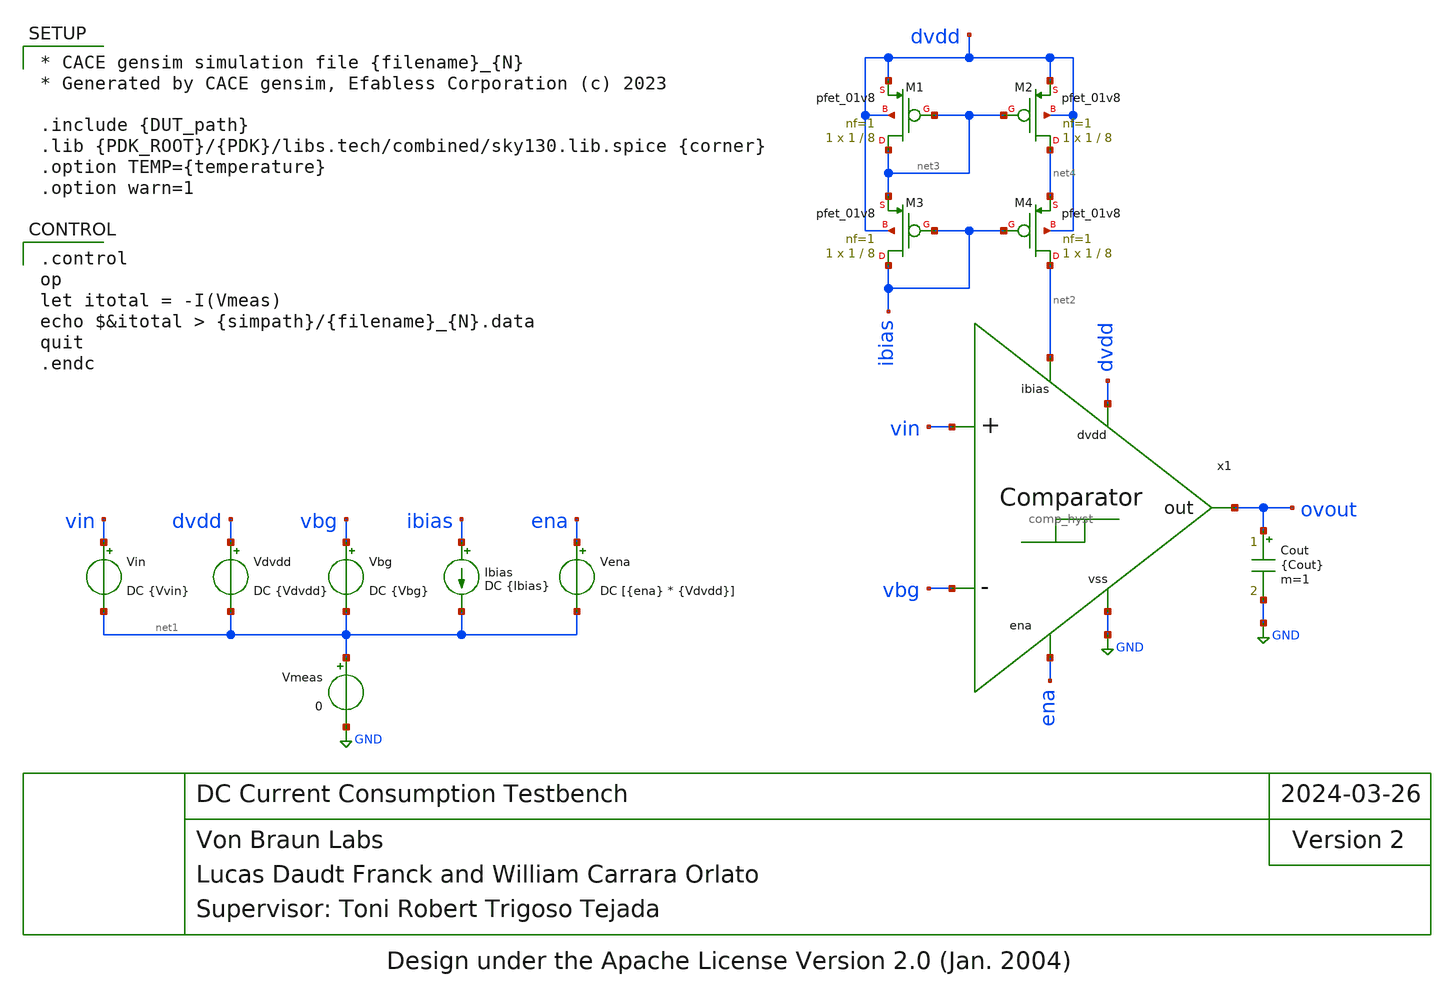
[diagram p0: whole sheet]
** sch_path: blocks/comp_hyst/cace/tb_dccurrent.sch
* Design under the Apache License Version 2.0 (Jan. 2004)
**.subckt tb_dccurrent
Cout ovout GND {Cout} m=1
Vin vin net1 DC {Vvin}
Vdvdd dvdd net1 DC {Vdvdd}
Vena ena net1 DC [{ena} * {Vdvdd}]
Vbg vbg net1 DC {Vbg}
Ibias ibias net1 DC {Ibias}
Vmeas net1 GND 0
XM1 net3 net3 dvdd dvdd sky130_fd_pr__pfet_01v8 L=8 W=1 nf=1 ad='int((nf+1)/2) * W/nf * 0.29' as='int((nf+2)/2) * W/nf * 0.29'
+ pd='2*int((nf+1)/2) * (W/nf + 0.29)' ps='2*int((nf+2)/2) * (W/nf + 0.29)' nrd='0.29 / W' nrs='0.29 / W'
+ sa=0 sb=0 sd=0 mult=1 m=1
XM2 net4 net3 dvdd dvdd sky130_fd_pr__pfet_01v8 L=8 W=1 nf=1 ad='int((nf+1)/2) * W/nf * 0.29' as='int((nf+2)/2) * W/nf * 0.29'
+ pd='2*int((nf+1)/2) * (W/nf + 0.29)' ps='2*int((nf+2)/2) * (W/nf + 0.29)' nrd='0.29 / W' nrs='0.29 / W'
+ sa=0 sb=0 sd=0 mult=1 m=1
XM3 ibias ibias net3 dvdd sky130_fd_pr__pfet_01v8 L=8 W=1 nf=1 ad='int((nf+1)/2) * W/nf * 0.29' as='int((nf+2)/2) * W/nf * 0.29'
+ pd='2*int((nf+1)/2) * (W/nf + 0.29)' ps='2*int((nf+2)/2) * (W/nf + 0.29)' nrd='0.29 / W' nrs='0.29 / W'
+ sa=0 sb=0 sd=0 mult=1 m=1
XM4 net2 ibias net4 dvdd sky130_fd_pr__pfet_01v8 L=8 W=1 nf=1 ad='int((nf+1)/2) * W/nf * 0.29' as='int((nf+2)/2) * W/nf * 0.29'
+ pd='2*int((nf+1)/2) * (W/nf + 0.29)' ps='2*int((nf+2)/2) * (W/nf + 0.29)' nrd='0.29 / W' nrs='0.29 / W'
+ sa=0 sb=0 sd=0 mult=1 m=1
x1 dvdd ovout vbg vin ena net2 GND comp_hyst
**** begin user architecture code

* CACE gensim simulation file {filename}_{N}
* Generated by CACE gensim, Efabless Corporation (c) 2023

.include {DUT_path}
.lib {PDK_ROOT}/{PDK}/libs.tech/combined/sky130.lib.spice {corner}
.option TEMP={temperature}
.option warn=1



.control
op
let itotal = -I(Vmeas)
echo $&itotal > {simpath}/{filename}_{N}.data
quit
.endc


**** end user architecture code
**.ends

* expanding   symbol:
*+  /home/vblabs/Music/sky130_vbl_ip__overvoltage/blocks/comp_hyst/xschem/comp_hyst.sym # of pins=7
** sym_path: blocks/comp_hyst/xschem/comp_hyst.sym
** sch_path: blocks/comp_hyst/xschem/comp_hyst.sch
.subckt comp_hyst dvdd out vref vin ena ibias vss
*.iopin dvdd
*.ipin vref
*.ipin vin
*.opin out
*.ipin ibias
*.ipin ena
*.iopin vss
XM5[0] net3 net4 dvdd dvdd sky130_fd_pr__pfet_01v8 L=8 W=1 nf=1 ad='int((nf+1)/2) * W/nf * 0.29' as='int((nf+2)/2) * W/nf * 0.29'
+ pd='2*int((nf+1)/2) * (W/nf + 0.29)' ps='2*int((nf+2)/2) * (W/nf + 0.29)' nrd='0.29 / W' nrs='0.29 / W'
+ sa=0 sb=0 sd=0 mult=1 m=1
XM5[1] net3 net4 dvdd dvdd sky130_fd_pr__pfet_01v8 L=8 W=1 nf=1 ad='int((nf+1)/2) * W/nf * 0.29' as='int((nf+2)/2) * W/nf * 0.29'
+ pd='2*int((nf+1)/2) * (W/nf + 0.29)' ps='2*int((nf+2)/2) * (W/nf + 0.29)' nrd='0.29 / W' nrs='0.29 / W'
+ sa=0 sb=0 sd=0 mult=1 m=1
XM2[0] net4 net4 dvdd dvdd sky130_fd_pr__pfet_01v8 L=8 W=1 nf=1 ad='int((nf+1)/2) * W/nf * 0.29' as='int((nf+2)/2) * W/nf * 0.29'
+ pd='2*int((nf+1)/2) * (W/nf + 0.29)' ps='2*int((nf+2)/2) * (W/nf + 0.29)' nrd='0.29 / W' nrs='0.29 / W'
+ sa=0 sb=0 sd=0 mult=1 m=1
XM2[1] net4 net4 dvdd dvdd sky130_fd_pr__pfet_01v8 L=8 W=1 nf=1 ad='int((nf+1)/2) * W/nf * 0.29' as='int((nf+2)/2) * W/nf * 0.29'
+ pd='2*int((nf+1)/2) * (W/nf + 0.29)' ps='2*int((nf+2)/2) * (W/nf + 0.29)' nrd='0.29 / W' nrs='0.29 / W'
+ sa=0 sb=0 sd=0 mult=1 m=1
XM8 net2 net4 dvdd dvdd sky130_fd_pr__pfet_01v8 L=8 W=1 nf=1 ad='int((nf+1)/2) * W/nf * 0.29' as='int((nf+2)/2) * W/nf * 0.29'
+ pd='2*int((nf+1)/2) * (W/nf + 0.29)' ps='2*int((nf+2)/2) * (W/nf + 0.29)' nrd='0.29 / W' nrs='0.29 / W'
+ sa=0 sb=0 sd=0 mult=1 m=1
XM10[0] net3 net3 dvdd dvdd sky130_fd_pr__pfet_01v8 L=16 W=1 nf=1 ad='int((nf+1)/2) * W/nf * 0.29' as='int((nf+2)/2) * W/nf * 0.29'
+ pd='2*int((nf+1)/2) * (W/nf + 0.29)' ps='2*int((nf+2)/2) * (W/nf + 0.29)' nrd='0.29 / W' nrs='0.29 / W'
+ sa=0 sb=0 sd=0 mult=1 m=1
XM10[1] net3 net3 dvdd dvdd sky130_fd_pr__pfet_01v8 L=16 W=1 nf=1 ad='int((nf+1)/2) * W/nf * 0.29' as='int((nf+2)/2) * W/nf * 0.29'
+ pd='2*int((nf+1)/2) * (W/nf + 0.29)' ps='2*int((nf+2)/2) * (W/nf + 0.29)' nrd='0.29 / W' nrs='0.29 / W'
+ sa=0 sb=0 sd=0 mult=1 m=1
XM11 net5 net5 vss vss sky130_fd_pr__nfet_01v8 L=20 W=1 nf=1 ad='int((nf+1)/2) * W/nf * 0.29' as='int((nf+2)/2) * W/nf * 0.29'
+ pd='2*int((nf+1)/2) * (W/nf + 0.29)' ps='2*int((nf+2)/2) * (W/nf + 0.29)' nrd='0.29 / W' nrs='0.29 / W'
+ sa=0 sb=0 sd=0 mult=1 m=1
XM12 net1 net5 vss vss sky130_fd_pr__nfet_01v8 L=20 W=1 nf=1 ad='int((nf+1)/2) * W/nf * 0.29' as='int((nf+2)/2) * W/nf * 0.29'
+ pd='2*int((nf+1)/2) * (W/nf + 0.29)' ps='2*int((nf+2)/2) * (W/nf + 0.29)' nrd='0.29 / W' nrs='0.29 / W'
+ sa=0 sb=0 sd=0 mult=1 m=1
XM4 out net3 dvdd dvdd sky130_fd_pr__pfet_01v8 L=1 W=3 nf=1 ad='int((nf+1)/2) * W/nf * 0.29' as='int((nf+2)/2) * W/nf * 0.29'
+ pd='2*int((nf+1)/2) * (W/nf + 0.29)' ps='2*int((nf+2)/2) * (W/nf + 0.29)' nrd='0.29 / W' nrs='0.29 / W'
+ sa=0 sb=0 sd=0 mult=1 m=1
XM13 out net2 vss vss sky130_fd_pr__nfet_01v8 L=1 W=3 nf=1 ad='int((nf+1)/2) * W/nf * 0.29' as='int((nf+2)/2) * W/nf * 0.29'
+ pd='2*int((nf+1)/2) * (W/nf + 0.29)' ps='2*int((nf+2)/2) * (W/nf + 0.29)' nrd='0.29 / W' nrs='0.29 / W'
+ sa=0 sb=0 sd=0 mult=1 m=1
XM20 out ena_b vss vss sky130_fd_pr__nfet_01v8 L=3 W=1 nf=1 ad='int((nf+1)/2) * W/nf * 0.29' as='int((nf+2)/2) * W/nf * 0.29'
+ pd='2*int((nf+1)/2) * (W/nf + 0.29)' ps='2*int((nf+2)/2) * (W/nf + 0.29)' nrd='0.29 / W' nrs='0.29 / W'
+ sa=0 sb=0 sd=0 mult=1 m=1
XM3[0] net4 vref net1 vss sky130_fd_pr__nfet_g5v0d10v5 L=8 W=1.3 nf=1 ad='int((nf+1)/2) * W/nf * 0.29'
+ as='int((nf+2)/2) * W/nf * 0.29' pd='2*int((nf+1)/2) * (W/nf + 0.29)' ps='2*int((nf+2)/2) * (W/nf + 0.29)'
+ nrd='0.29 / W' nrs='0.29 / W' sa=0 sb=0 sd=0 mult=1 m=1
XM3[1] net4 vref net1 vss sky130_fd_pr__nfet_g5v0d10v5 L=8 W=1.3 nf=1 ad='int((nf+1)/2) * W/nf * 0.29'
+ as='int((nf+2)/2) * W/nf * 0.29' pd='2*int((nf+1)/2) * (W/nf + 0.29)' ps='2*int((nf+2)/2) * (W/nf + 0.29)'
+ nrd='0.29 / W' nrs='0.29 / W' sa=0 sb=0 sd=0 mult=1 m=1
XM4[0] net3 vin net1 vss sky130_fd_pr__nfet_g5v0d10v5 L=8 W=1.3 nf=1 ad='int((nf+1)/2) * W/nf * 0.29'
+ as='int((nf+2)/2) * W/nf * 0.29' pd='2*int((nf+1)/2) * (W/nf + 0.29)' ps='2*int((nf+2)/2) * (W/nf + 0.29)'
+ nrd='0.29 / W' nrs='0.29 / W' sa=0 sb=0 sd=0 mult=1 m=1
XM4[1] net3 vin net1 vss sky130_fd_pr__nfet_g5v0d10v5 L=8 W=1.3 nf=1 ad='int((nf+1)/2) * W/nf * 0.29'
+ as='int((nf+2)/2) * W/nf * 0.29' pd='2*int((nf+1)/2) * (W/nf + 0.29)' ps='2*int((nf+2)/2) * (W/nf + 0.29)'
+ nrd='0.29 / W' nrs='0.29 / W' sa=0 sb=0 sd=0 mult=1 m=1
XM3 net5 ena_b vss vss sky130_fd_pr__nfet_01v8 L=3 W=1 nf=1 ad='int((nf+1)/2) * W/nf * 0.29' as='int((nf+2)/2) * W/nf * 0.29'
+ pd='2*int((nf+1)/2) * (W/nf + 0.29)' ps='2*int((nf+2)/2) * (W/nf + 0.29)' nrd='0.29 / W' nrs='0.29 / W'
+ sa=0 sb=0 sd=0 mult=1 m=1
XM1[0] net4 net3 dvdd dvdd sky130_fd_pr__pfet_01v8 L=16 W=1 nf=1 ad='int((nf+1)/2) * W/nf * 0.29' as='int((nf+2)/2) * W/nf * 0.29'
+ pd='2*int((nf+1)/2) * (W/nf + 0.29)' ps='2*int((nf+2)/2) * (W/nf + 0.29)' nrd='0.29 / W' nrs='0.29 / W'
+ sa=0 sb=0 sd=0 mult=1 m=1
XM1[1] net4 net3 dvdd dvdd sky130_fd_pr__pfet_01v8 L=16 W=1 nf=1 ad='int((nf+1)/2) * W/nf * 0.29' as='int((nf+2)/2) * W/nf * 0.29'
+ pd='2*int((nf+1)/2) * (W/nf + 0.29)' ps='2*int((nf+2)/2) * (W/nf + 0.29)' nrd='0.29 / W' nrs='0.29 / W'
+ sa=0 sb=0 sd=0 mult=1 m=1
XM1[2] net4 net3 dvdd dvdd sky130_fd_pr__pfet_01v8 L=16 W=1 nf=1 ad='int((nf+1)/2) * W/nf * 0.29' as='int((nf+2)/2) * W/nf * 0.29'
+ pd='2*int((nf+1)/2) * (W/nf + 0.29)' ps='2*int((nf+2)/2) * (W/nf + 0.29)' nrd='0.29 / W' nrs='0.29 / W'
+ sa=0 sb=0 sd=0 mult=1 m=1
XM1[3] net4 net3 dvdd dvdd sky130_fd_pr__pfet_01v8 L=16 W=1 nf=1 ad='int((nf+1)/2) * W/nf * 0.29' as='int((nf+2)/2) * W/nf * 0.29'
+ pd='2*int((nf+1)/2) * (W/nf + 0.29)' ps='2*int((nf+2)/2) * (W/nf + 0.29)' nrd='0.29 / W' nrs='0.29 / W'
+ sa=0 sb=0 sd=0 mult=1 m=1
XM9 net2 net2 vss vss sky130_fd_pr__nfet_01v8 L=8 W=1 nf=1 ad='int((nf+1)/2) * W/nf * 0.29' as='int((nf+2)/2) * W/nf * 0.29'
+ pd='2*int((nf+1)/2) * (W/nf + 0.29)' ps='2*int((nf+2)/2) * (W/nf + 0.29)' nrd='0.29 / W' nrs='0.29 / W'
+ sa=0 sb=0 sd=0 mult=1 m=1
XM5 net3 ena dvdd dvdd sky130_fd_pr__pfet_01v8 L=3 W=1 nf=1 ad='int((nf+1)/2) * W/nf * 0.29' as='int((nf+2)/2) * W/nf * 0.29'
+ pd='2*int((nf+1)/2) * (W/nf + 0.29)' ps='2*int((nf+2)/2) * (W/nf + 0.29)' nrd='0.29 / W' nrs='0.29 / W'
+ sa=0 sb=0 sd=0 mult=1 m=1
XM14 net4 ena dvdd dvdd sky130_fd_pr__pfet_01v8 L=3 W=1 nf=1 ad='int((nf+1)/2) * W/nf * 0.29' as='int((nf+2)/2) * W/nf * 0.29'
+ pd='2*int((nf+1)/2) * (W/nf + 0.29)' ps='2*int((nf+2)/2) * (W/nf + 0.29)' nrd='0.29 / W' nrs='0.29 / W'
+ sa=0 sb=0 sd=0 mult=1 m=1
XM15 net2 ena_b vss vss sky130_fd_pr__nfet_01v8 L=3 W=1 nf=1 ad='int((nf+1)/2) * W/nf * 0.29' as='int((nf+2)/2) * W/nf * 0.29'
+ pd='2*int((nf+1)/2) * (W/nf + 0.29)' ps='2*int((nf+2)/2) * (W/nf + 0.29)' nrd='0.29 / W' nrs='0.29 / W'
+ sa=0 sb=0 sd=0 mult=1 m=1
XM1 ena_b ena dvdd dvdd sky130_fd_pr__pfet_01v8 L=3 W=1 nf=1 ad='int((nf+1)/2) * W/nf * 0.29' as='int((nf+2)/2) * W/nf * 0.29'
+ pd='2*int((nf+1)/2) * (W/nf + 0.29)' ps='2*int((nf+2)/2) * (W/nf + 0.29)' nrd='0.29 / W' nrs='0.29 / W'
+ sa=0 sb=0 sd=0 mult=1 m=1
XM2 ena_b ena vss vss sky130_fd_pr__nfet_01v8 L=3 W=1 nf=1 ad='int((nf+1)/2) * W/nf * 0.29' as='int((nf+2)/2) * W/nf * 0.29'
+ pd='2*int((nf+1)/2) * (W/nf + 0.29)' ps='2*int((nf+2)/2) * (W/nf + 0.29)' nrd='0.29 / W' nrs='0.29 / W'
+ sa=0 sb=0 sd=0 mult=1 m=1
x1 ibias ena ena_b dvdd vss net5 trans_gate
.ends


* expanding   symbol:  trans_gate.sym # of pins=6
** sym_path: blocks/comp_hyst/xschem/trans_gate.sym
** sch_path: blocks/comp_hyst/xschem/trans_gate.sch
.subckt trans_gate in ena_b ena avdd vss out
*.iopin avdd
*.iopin vss
*.ipin ena
*.ipin ena_b
*.ipin in
*.ipin out
XM1 in ena_b out vss sky130_fd_pr__nfet_g5v0d10v5 L=5 W=1 nf=1 ad='int((nf+1)/2) * W/nf * 0.29' as='int((nf+2)/2) * W/nf * 0.29'
+ pd='2*int((nf+1)/2) * (W/nf + 0.29)' ps='2*int((nf+2)/2) * (W/nf + 0.29)' nrd='0.29 / W' nrs='0.29 / W'
+ sa=0 sb=0 sd=0 mult=1 m=1
XM2 in ena out avdd sky130_fd_pr__pfet_g5v0d10v5 L=5 W=6 nf=1 ad='int((nf+1)/2) * W/nf * 0.29' as='int((nf+2)/2) * W/nf * 0.29'
+ pd='2*int((nf+1)/2) * (W/nf + 0.29)' ps='2*int((nf+2)/2) * (W/nf + 0.29)' nrd='0.29 / W' nrs='0.29 / W'
+ sa=0 sb=0 sd=0 mult=1 m=1
.ends

.GLOBAL GND
.end
